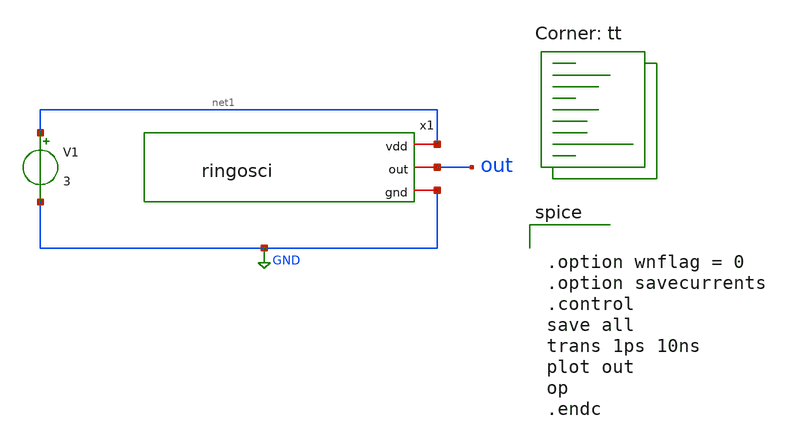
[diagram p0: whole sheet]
** sch_path: ringosci/ringosci_tb.sch
**.subckt ringosci_tb
x1 net1 out GND ringosci
V1 net1 GND 3
**** begin user architecture code


.option wnflag = 0
.option savecurrents
.control
save all
trans 1ps 10ns
plot out
op
.endc

.lib $::SKYWATER_MODELS/sky130.lib.spice tt
**** end user architecture code
**.ends
.GLOBAL GND
.end
